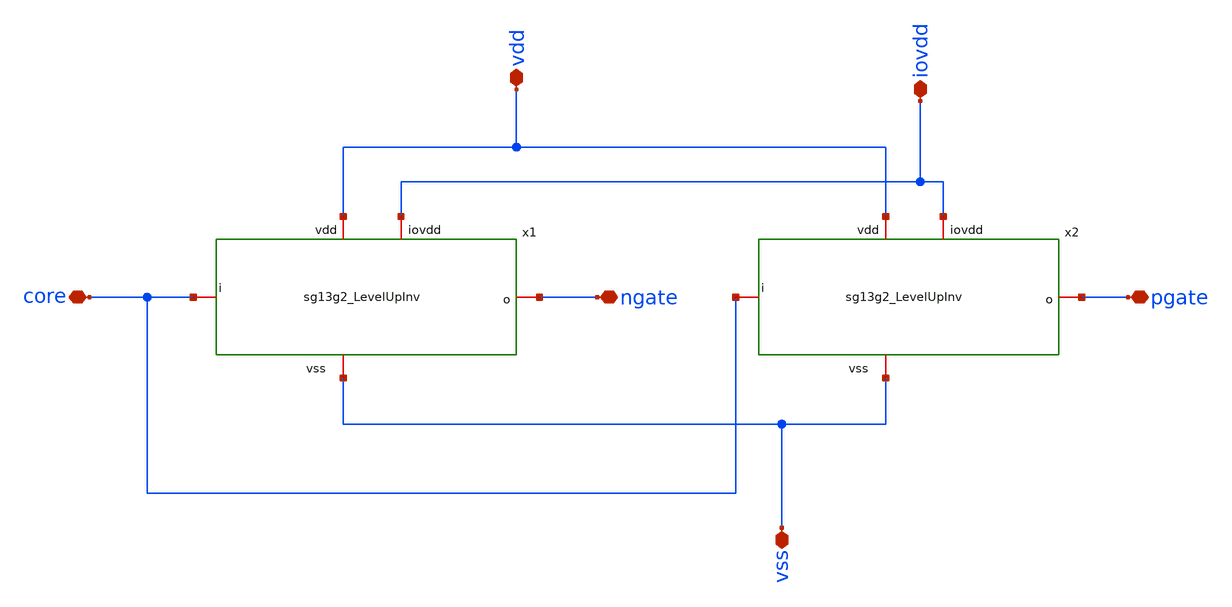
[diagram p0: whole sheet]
** sch_path: CDR4176-main/schematic/xschem/project_io/sg13g2_GateLevelUpInv/sg13g2_GateLevelUpInv.sch
**.subckt sg13g2_GateLevelUpInv vdd iovdd core vss pgate ngate
*.iopin vdd
*.iopin iovdd
*.iopin core
*.iopin vss
*.iopin pgate
*.iopin ngate
x1 iovdd vdd ngate core vss sg13g2_LevelUpInv
x2 iovdd vdd pgate core vss sg13g2_LevelUpInv
**.ends
.end
